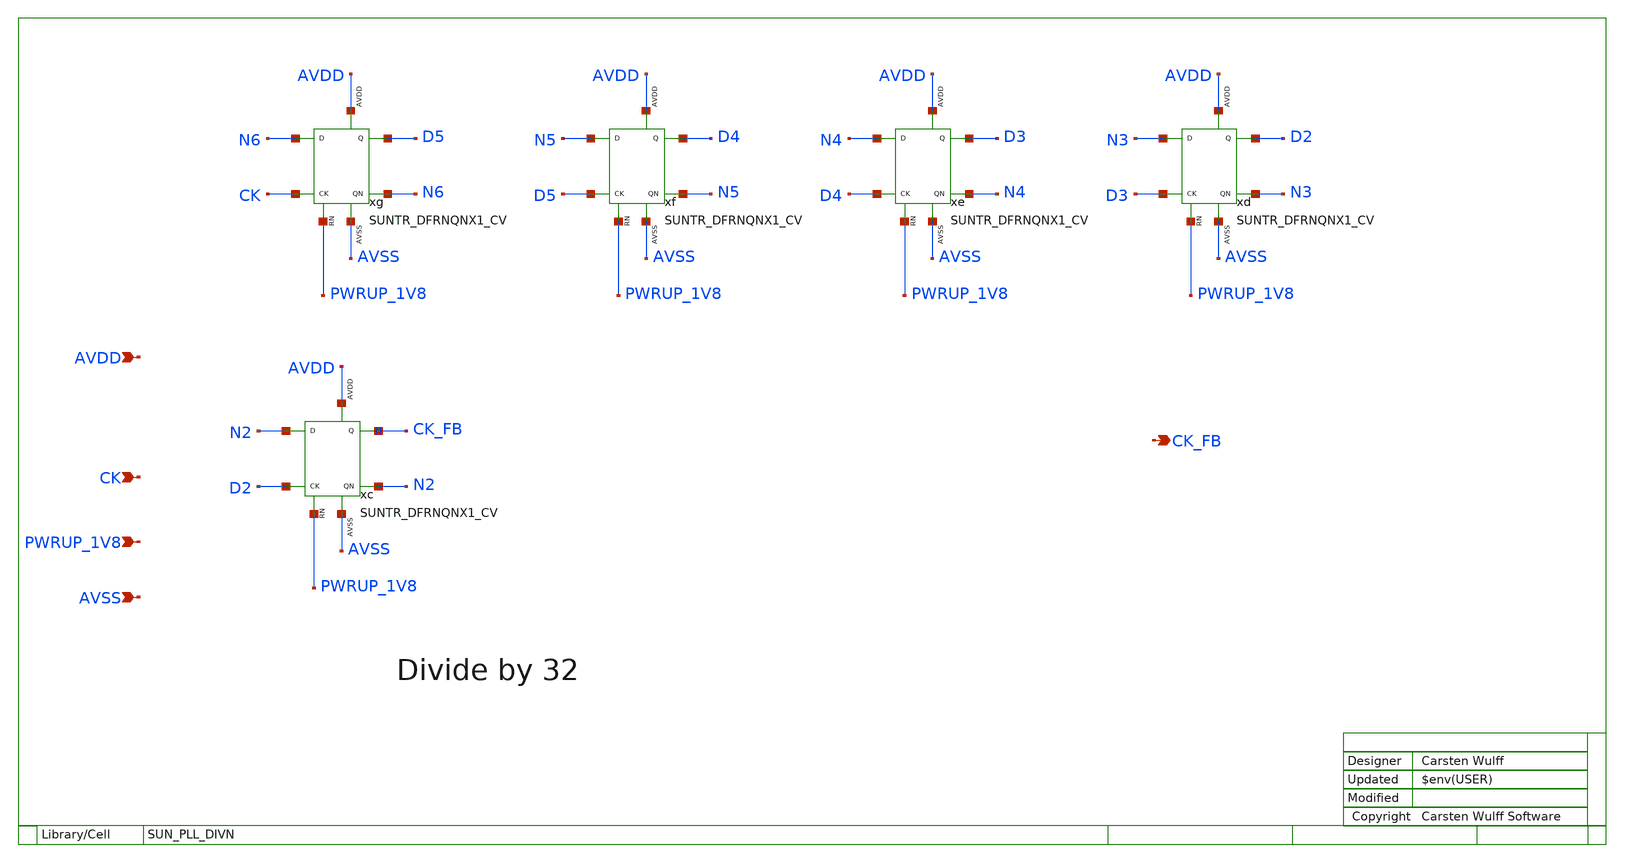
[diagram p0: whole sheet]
** sch_path: ip/sun_pll_sky130nm/design/SUN_PLL_SKY130NM/SUN_PLL_DIVN.sch
**.subckt SUN_PLL_DIVN PWRUP_1V8 CK AVDD AVSS CK_FB
*.ipin PWRUP_1V8
*.ipin CK
*.ipin AVDD
*.ipin AVSS
*.opin CK_FB
xg N6 CK PWRUP_1V8 D5 N6 AVDD AVSS SUNTR_DFRNQNX1_CV xoffset=0 yoffset=0 angle=0
xf N5 D5 PWRUP_1V8 D4 N5 AVDD AVSS SUNTR_DFRNQNX1_CV xoffset=0 yoffset=0 angle=0
xe N4 D4 PWRUP_1V8 D3 N4 AVDD AVSS SUNTR_DFRNQNX1_CV xoffset=0 yoffset=0 angle=0
xd N3 D3 PWRUP_1V8 D2 N3 AVDD AVSS SUNTR_DFRNQNX1_CV xoffset=0 yoffset=0 angle=0
xc N2 D2 PWRUP_1V8 CK_FB N2 AVDD AVSS SUNTR_DFRNQNX1_CV xoffset=0 yoffset=0 angle=0
**.ends
.end
